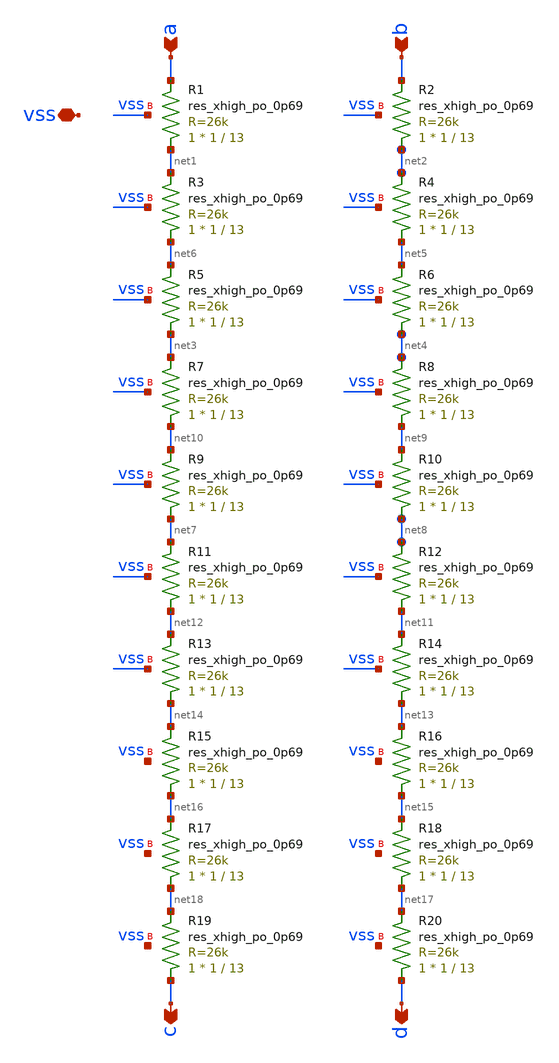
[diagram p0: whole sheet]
** sch_path: xschem/bandgap/bg_res.sch
**.subckt bg_res a b c d vss
*.ipin a
*.ipin b
*.opin c
*.opin d
*.iopin vss
XR1 net1 a vss sky130_fd_pr__res_xhigh_po_0p69 W=1 L=13 mult=1 m=1
XR2 net2 b vss sky130_fd_pr__res_xhigh_po_0p69 W=1 L=13 mult=1 m=1
XR3 net6 net1 vss sky130_fd_pr__res_xhigh_po_0p69 W=1 L=13 mult=1 m=1
XR4 net5 net2 vss sky130_fd_pr__res_xhigh_po_0p69 W=1 L=13 mult=1 m=1
XR5 net3 net6 vss sky130_fd_pr__res_xhigh_po_0p69 W=1 L=13 mult=1 m=1
XR6 net4 net5 vss sky130_fd_pr__res_xhigh_po_0p69 W=1 L=13 mult=1 m=1
XR7 net10 net3 vss sky130_fd_pr__res_xhigh_po_0p69 W=1 L=13 mult=1 m=1
XR8 net9 net4 vss sky130_fd_pr__res_xhigh_po_0p69 W=1 L=13 mult=1 m=1
XR9 net7 net10 vss sky130_fd_pr__res_xhigh_po_0p69 W=1 L=13 mult=1 m=1
XR10 net8 net9 vss sky130_fd_pr__res_xhigh_po_0p69 W=1 L=13 mult=1 m=1
XR11 net12 net7 vss sky130_fd_pr__res_xhigh_po_0p69 W=1 L=13 mult=1 m=1
XR12 net11 net8 vss sky130_fd_pr__res_xhigh_po_0p69 W=1 L=13 mult=1 m=1
XR13 net14 net12 vss sky130_fd_pr__res_xhigh_po_0p69 W=1 L=13 mult=1 m=1
XR14 net13 net11 vss sky130_fd_pr__res_xhigh_po_0p69 W=1 L=13 mult=1 m=1
XR15 net16 net14 vss sky130_fd_pr__res_xhigh_po_0p69 W=1 L=13 mult=1 m=1
XR16 net15 net13 vss sky130_fd_pr__res_xhigh_po_0p69 W=1 L=13 mult=1 m=1
XR17 net18 net16 vss sky130_fd_pr__res_xhigh_po_0p69 W=1 L=13 mult=1 m=1
XR18 net17 net15 vss sky130_fd_pr__res_xhigh_po_0p69 W=1 L=13 mult=1 m=1
XR19 c net18 vss sky130_fd_pr__res_xhigh_po_0p69 W=1 L=13 mult=1 m=1
XR20 d net17 vss sky130_fd_pr__res_xhigh_po_0p69 W=1 L=13 mult=1 m=1
**.ends
.end
